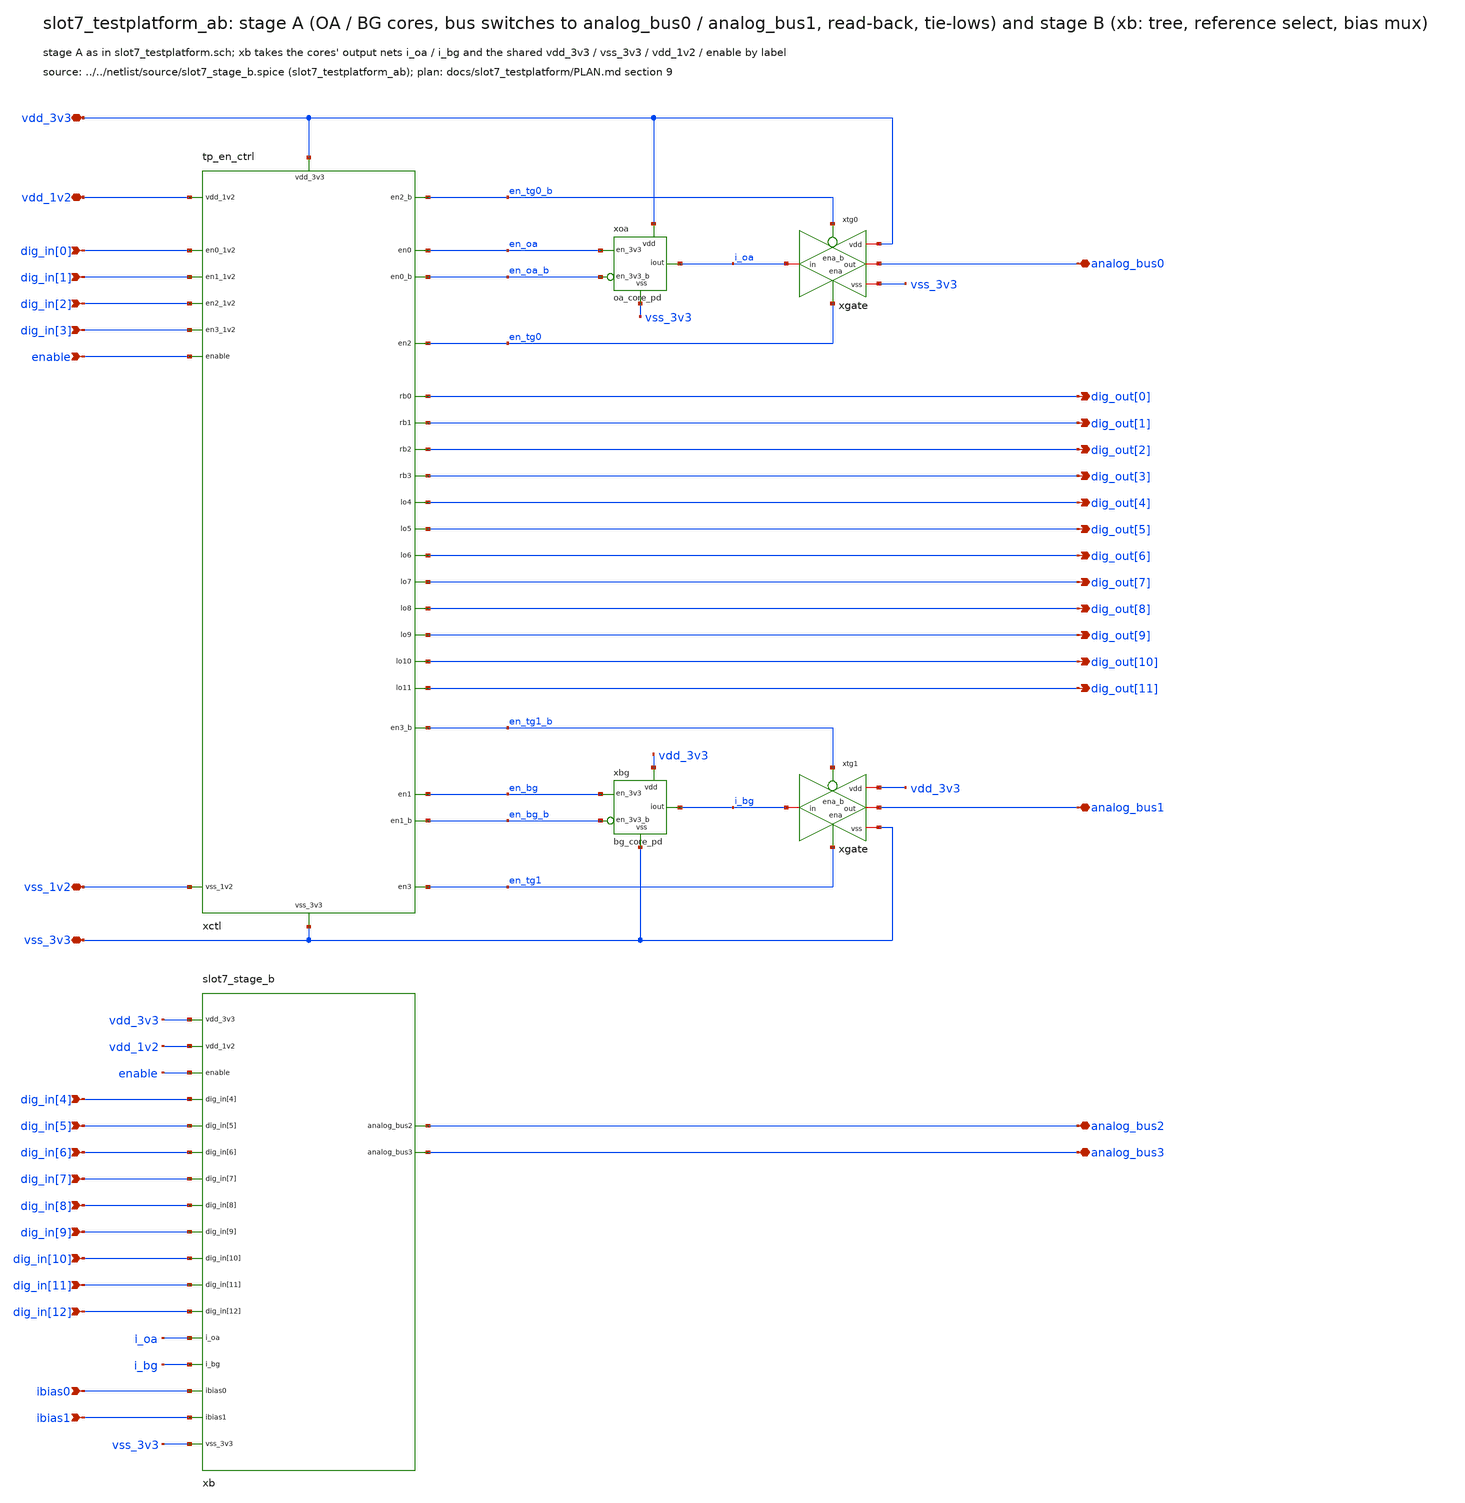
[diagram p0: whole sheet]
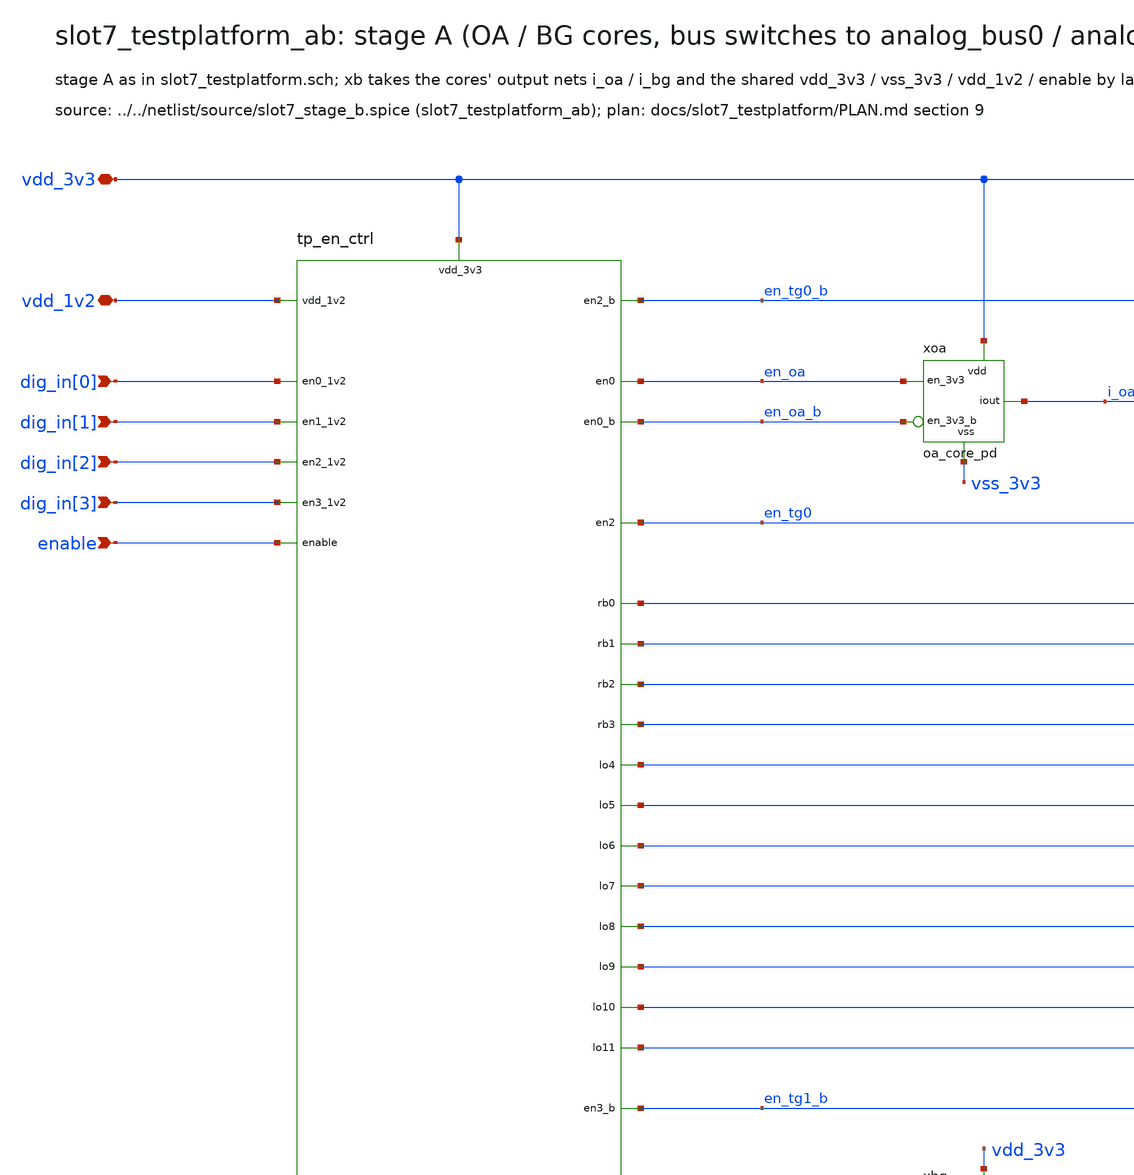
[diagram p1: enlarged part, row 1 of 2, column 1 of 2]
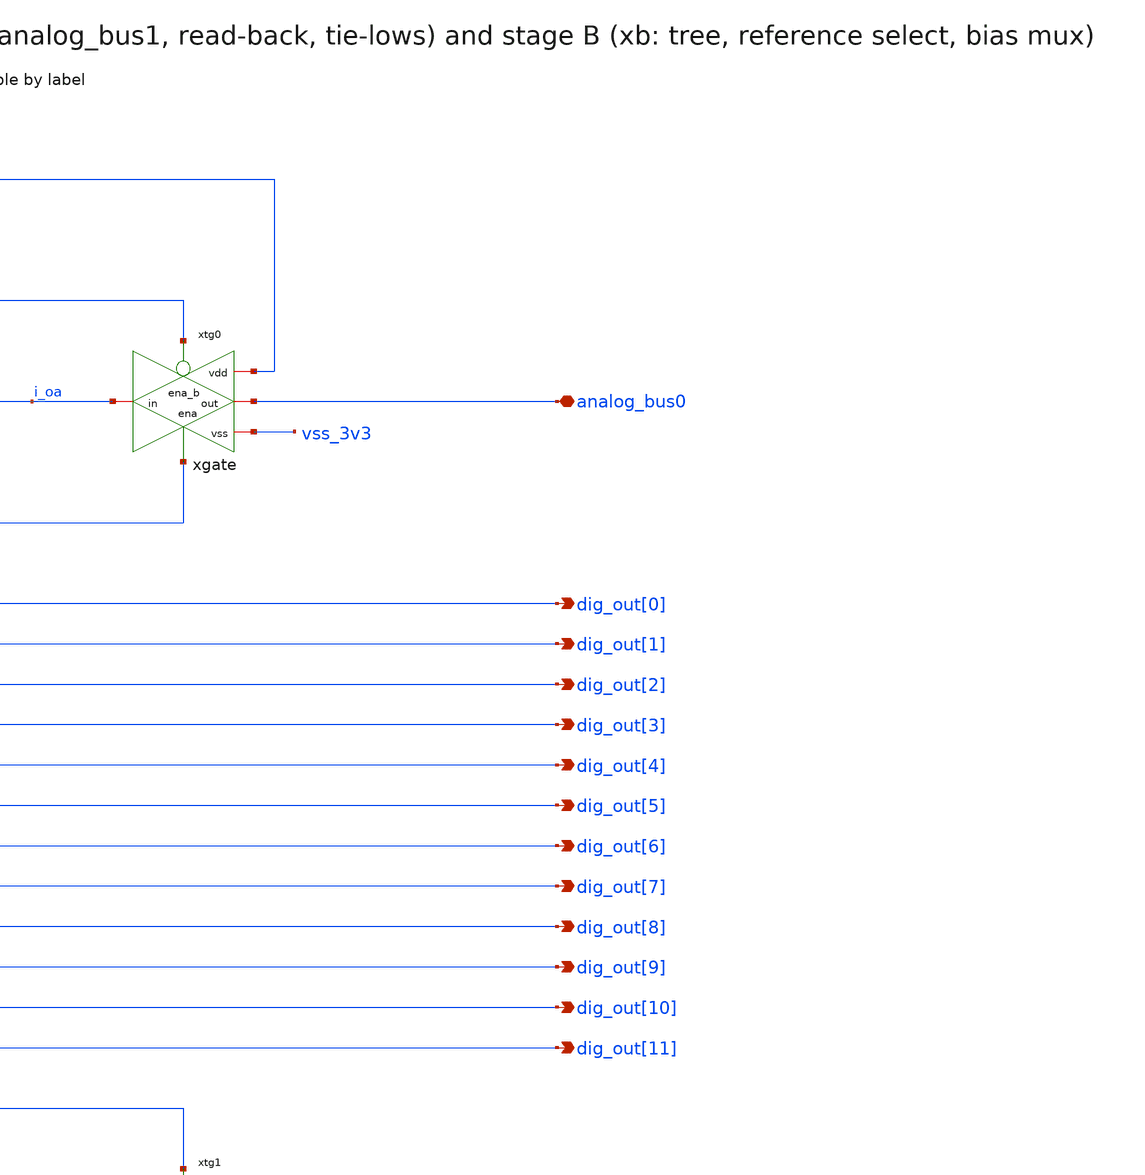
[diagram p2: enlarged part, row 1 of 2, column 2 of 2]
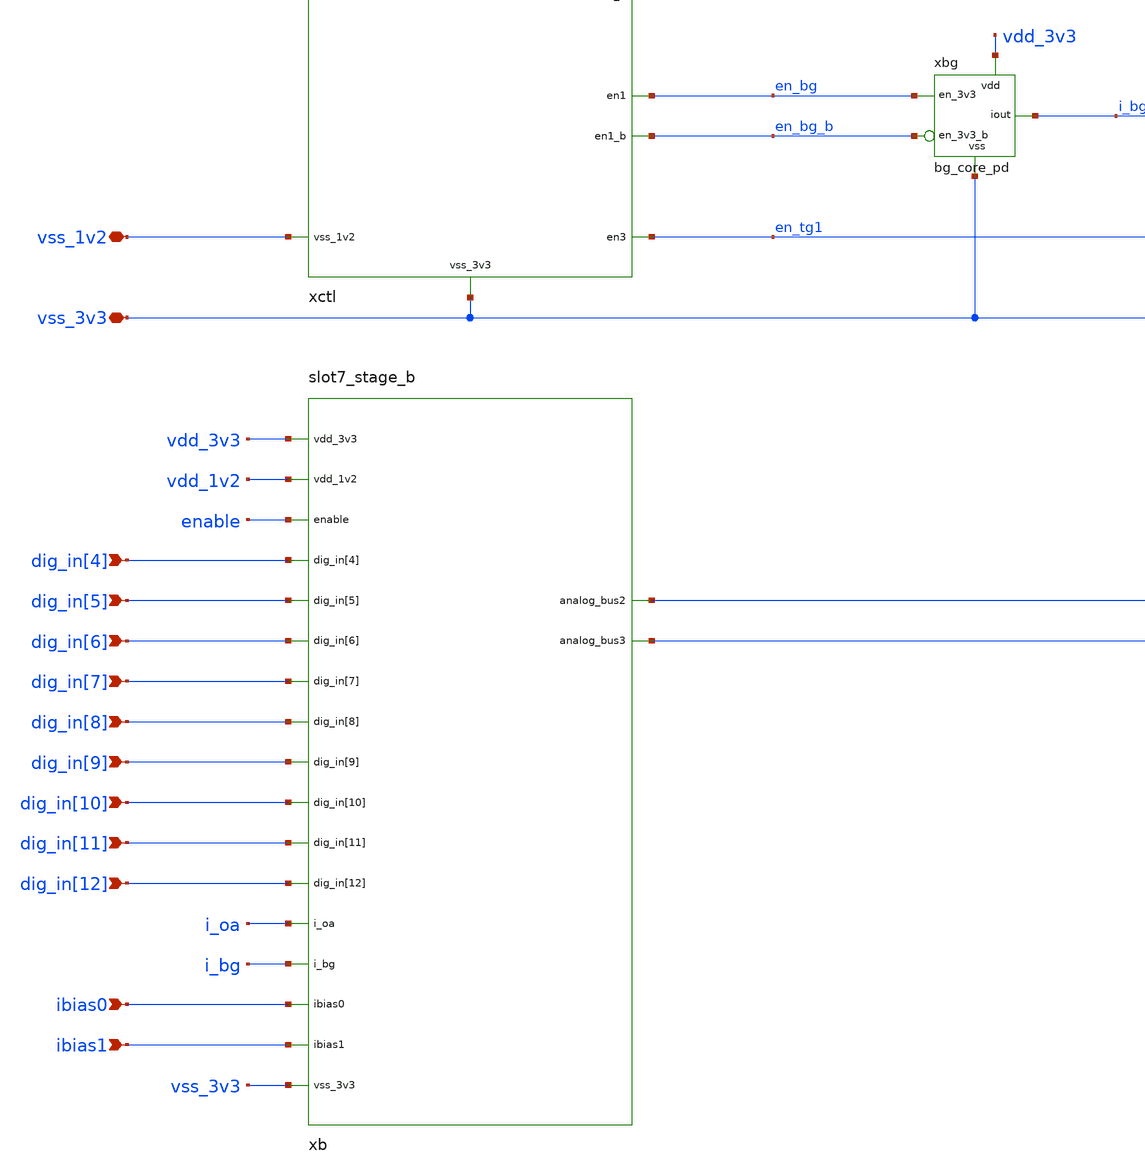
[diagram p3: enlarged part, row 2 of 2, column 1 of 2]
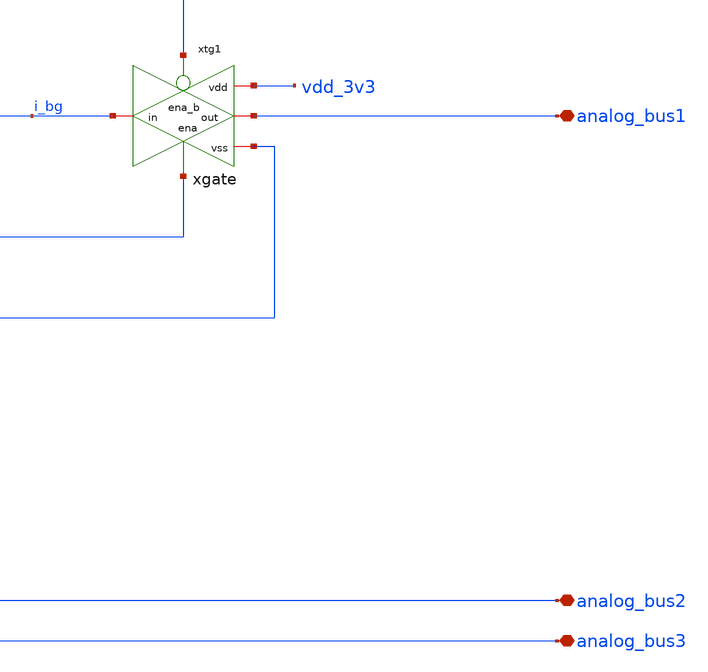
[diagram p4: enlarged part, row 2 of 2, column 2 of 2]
** sch_path: macros/slot7_testplatform/schematic/xschem_drawn/slot7_testplatform_ab.sch
**.subckt slot7_testplatform_ab vdd_3v3 vss_3v3 vdd_1v2 vss_1v2 enable dig_in[0] dig_in[1] dig_in[2]
*+ dig_in[3] dig_in[4] dig_in[5] dig_in[6] dig_in[7] dig_in[8] dig_in[9] dig_in[10] dig_in[11] dig_in[12]
*+ dig_out[0] dig_out[1] dig_out[2] dig_out[3] dig_out[4] dig_out[5] dig_out[6] dig_out[7] dig_out[8] dig_out[9]
*+ dig_out[10] dig_out[11] analog_bus0 analog_bus1 analog_bus2 analog_bus3 ibias0 ibias1
*.iopin vdd_3v3
*.iopin vss_3v3
*.iopin vdd_1v2
*.iopin vss_1v2
*.ipin enable
*.ipin dig_in[0]
*.ipin dig_in[1]
*.ipin dig_in[2]
*.ipin dig_in[3]
*.ipin dig_in[4]
*.ipin dig_in[5]
*.ipin dig_in[6]
*.ipin dig_in[7]
*.ipin dig_in[8]
*.ipin dig_in[9]
*.ipin dig_in[10]
*.ipin dig_in[11]
*.ipin dig_in[12]
*.opin dig_out[0]
*.opin dig_out[1]
*.opin dig_out[2]
*.opin dig_out[3]
*.opin dig_out[4]
*.opin dig_out[5]
*.opin dig_out[6]
*.opin dig_out[7]
*.opin dig_out[8]
*.opin dig_out[9]
*.opin dig_out[10]
*.opin dig_out[11]
*.iopin analog_bus0
*.iopin analog_bus1
*.iopin analog_bus2
*.iopin analog_bus3
*.ipin ibias0
*.ipin ibias1
xctl vdd_3v3 vss_3v3 vdd_1v2 vss_1v2 dig_in[0] dig_in[1] dig_in[2] dig_in[3] enable en_oa en_oa_b
+ en_bg en_bg_b en_tg0 en_tg0_b en_tg1 en_tg1_b dig_out[0] dig_out[1] dig_out[2] dig_out[3] dig_out[4]
+ dig_out[5] dig_out[6] dig_out[7] dig_out[8] dig_out[9] dig_out[10] dig_out[11] tp_en_ctrl
xoa vdd_3v3 vss_3v3 i_oa en_oa en_oa_b oa_core_pd
xtg0 en_tg0_b vdd_3v3 i_oa analog_bus0 vss_3v3 en_tg0 xgate
xbg vdd_3v3 vss_3v3 i_bg en_bg en_bg_b bg_core_pd
xtg1 en_tg1_b vdd_3v3 i_bg analog_bus1 vss_3v3 en_tg1 xgate
xb vdd_3v3 vss_3v3 vdd_1v2 enable dig_in[4] dig_in[5] dig_in[6] dig_in[7] dig_in[8] dig_in[9]
+ dig_in[10] dig_in[11] dig_in[12] i_oa i_bg ibias0 ibias1 analog_bus2 analog_bus3 slot7_stage_b
**.ends
.end
